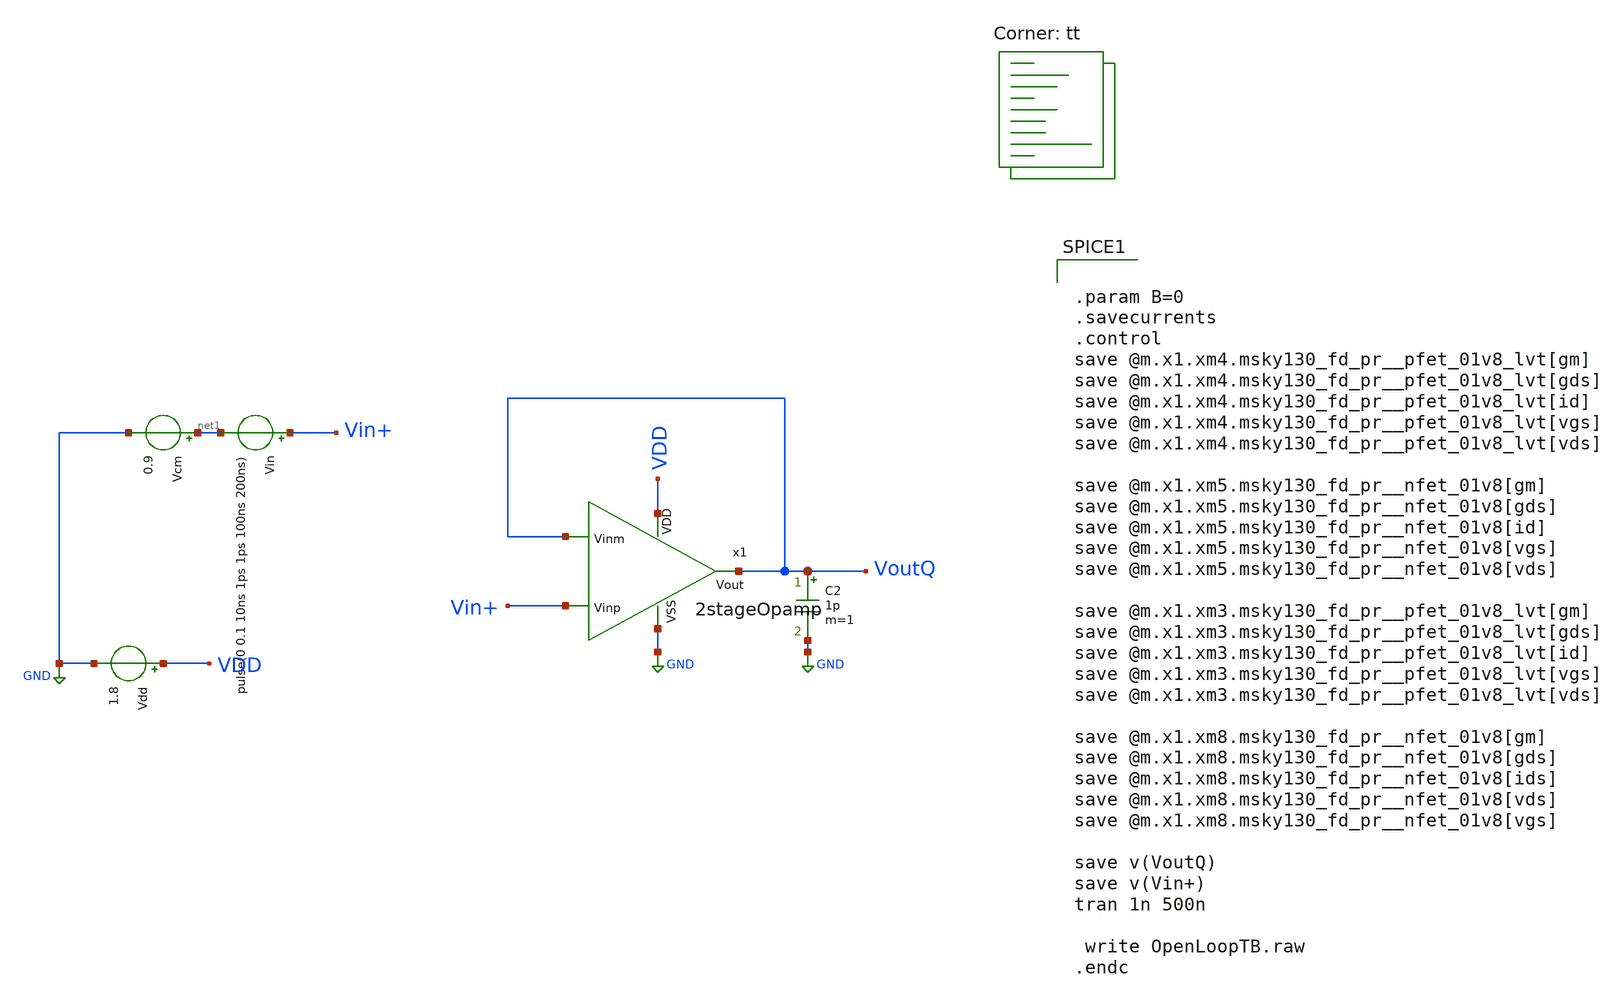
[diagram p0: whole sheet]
** sch_path: xschem/TestBenches/TranTB.sch
**.subckt TranTB
C2 VoutQ GND 1p m=1
x1 VDD VoutQ Vin+ VoutQ GND 2stageOpamp
Vdd VDD GND 1.8
.save i(vdd)
Vin Vin+ net1 pulse(0 0.1 10ns 1ps 1ps 100ns 200ns)
Vcm net1 GND 0.9
**** begin user architecture code


.param B=0
.savecurrents
.control
save @m.x1.xm4.msky130_fd_pr__pfet_01v8_lvt[gm]
save @m.x1.xm4.msky130_fd_pr__pfet_01v8_lvt[gds]
save @m.x1.xm4.msky130_fd_pr__pfet_01v8_lvt[id]
save @m.x1.xm4.msky130_fd_pr__pfet_01v8_lvt[vgs]
save @m.x1.xm4.msky130_fd_pr__pfet_01v8_lvt[vds]

save @m.x1.xm5.msky130_fd_pr__nfet_01v8[gm]
save @m.x1.xm5.msky130_fd_pr__nfet_01v8[gds]
save @m.x1.xm5.msky130_fd_pr__nfet_01v8[id]
save @m.x1.xm5.msky130_fd_pr__nfet_01v8[vgs]
save @m.x1.xm5.msky130_fd_pr__nfet_01v8[vds]

save @m.x1.xm3.msky130_fd_pr__pfet_01v8_lvt[gm]
save @m.x1.xm3.msky130_fd_pr__pfet_01v8_lvt[gds]
save @m.x1.xm3.msky130_fd_pr__pfet_01v8_lvt[id]
save @m.x1.xm3.msky130_fd_pr__pfet_01v8_lvt[vgs]
save @m.x1.xm3.msky130_fd_pr__pfet_01v8_lvt[vds]

save @m.x1.xm8.msky130_fd_pr__nfet_01v8[gm]
save @m.x1.xm8.msky130_fd_pr__nfet_01v8[gds]
save @m.x1.xm8.msky130_fd_pr__nfet_01v8[ids]
save @m.x1.xm8.msky130_fd_pr__nfet_01v8[vds]
save @m.x1.xm8.msky130_fd_pr__nfet_01v8[vgs]

save v(VoutQ)
save v(Vin+)
tran 1n 500n

 write OpenLoopTB.raw
.endc


.lib $::SKYWATER_MODELS/sky130.lib.spice tt
**** end user architecture code
**.ends
.GLOBAL GND
.end
